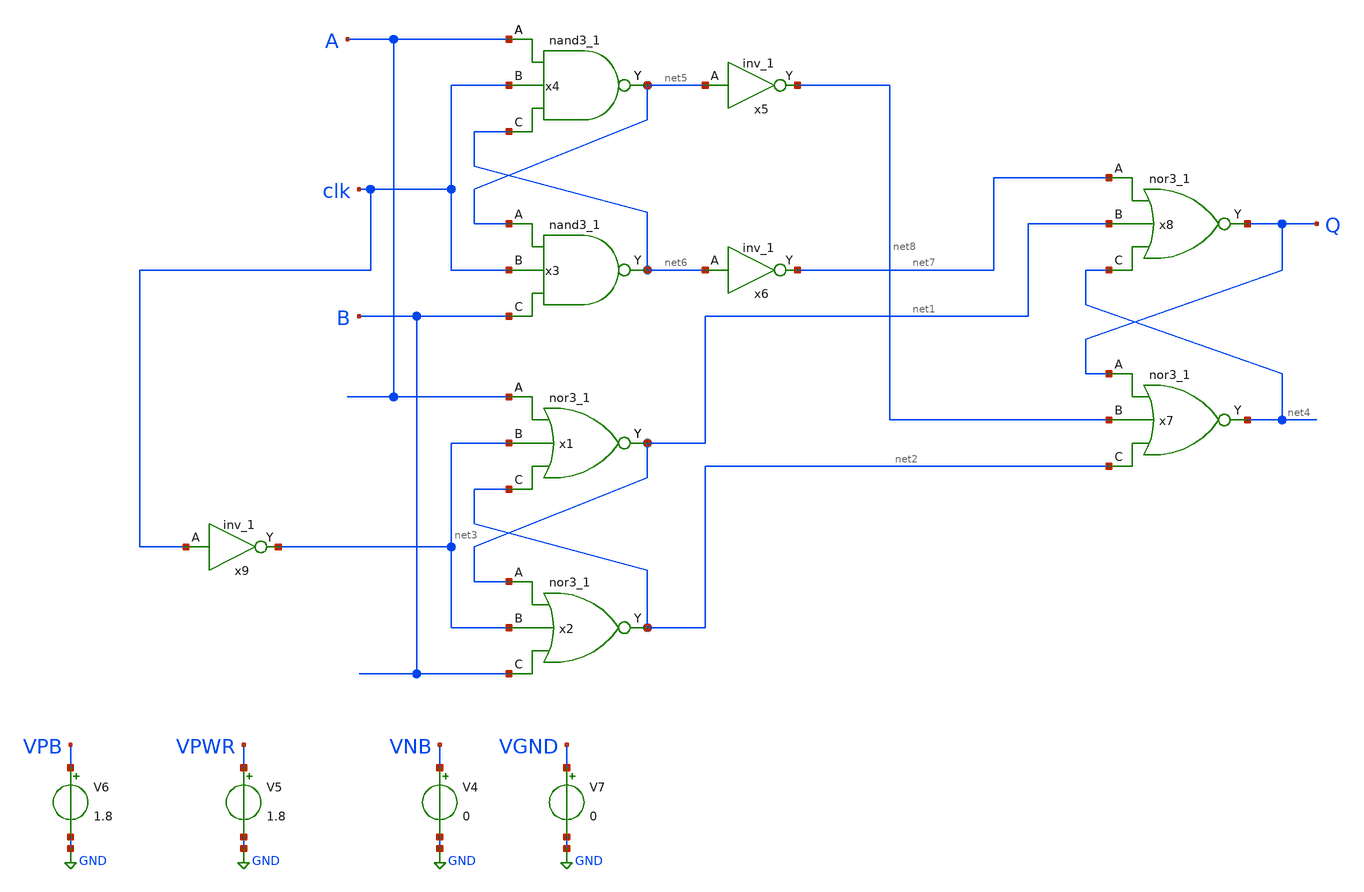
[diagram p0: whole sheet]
** sch_path: cmp/NandNorcmp.sch
**.subckt NandNorcmp
x1 A net3 net2 VGND VNB VPB VPWR net1 sky130_fd_sc_hd__nor3_1
x2 net1 net3 B VGND VNB VPB VPWR net2 sky130_fd_sc_hd__nor3_1
V4 VNB GND 0
V5 VPWR GND 1.8
V6 VPB GND 1.8
V7 VGND GND 0
x3 net5 clk B VGND VNB VPB VPWR net6 sky130_fd_sc_hd__nand3_1
x4 A clk net6 VGND VNB VPB VPWR net5 sky130_fd_sc_hd__nand3_1
x5 net5 VGND VNB VPB VPWR net8 sky130_fd_sc_hd__inv_1
x6 net6 VGND VNB VPB VPWR net7 sky130_fd_sc_hd__inv_1
x7 Q net8 net2 VGND VNB VPB VPWR net4 sky130_fd_sc_hd__nor3_1
x8 net7 net1 net4 VGND VNB VPB VPWR Q sky130_fd_sc_hd__nor3_1
x9 clk VGND VNB VPB VPWR net3 sky130_fd_sc_hd__inv_1
**.ends
.GLOBAL GND
.end
